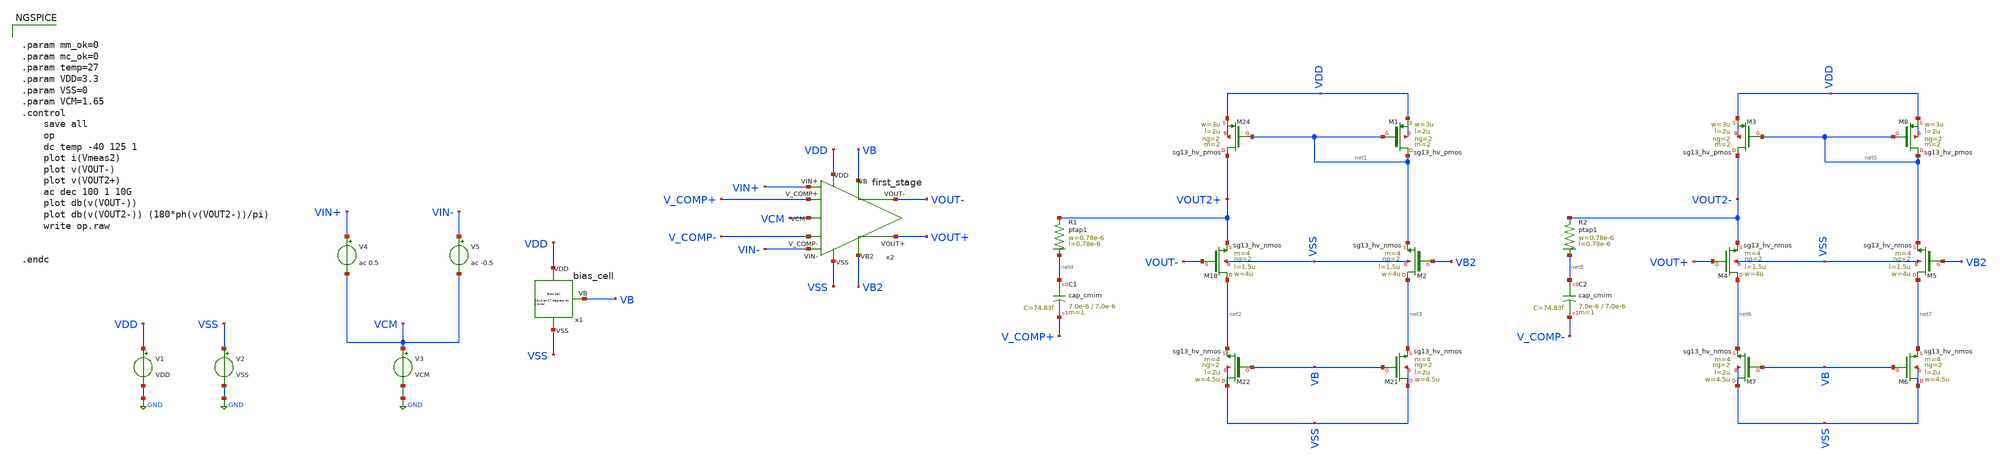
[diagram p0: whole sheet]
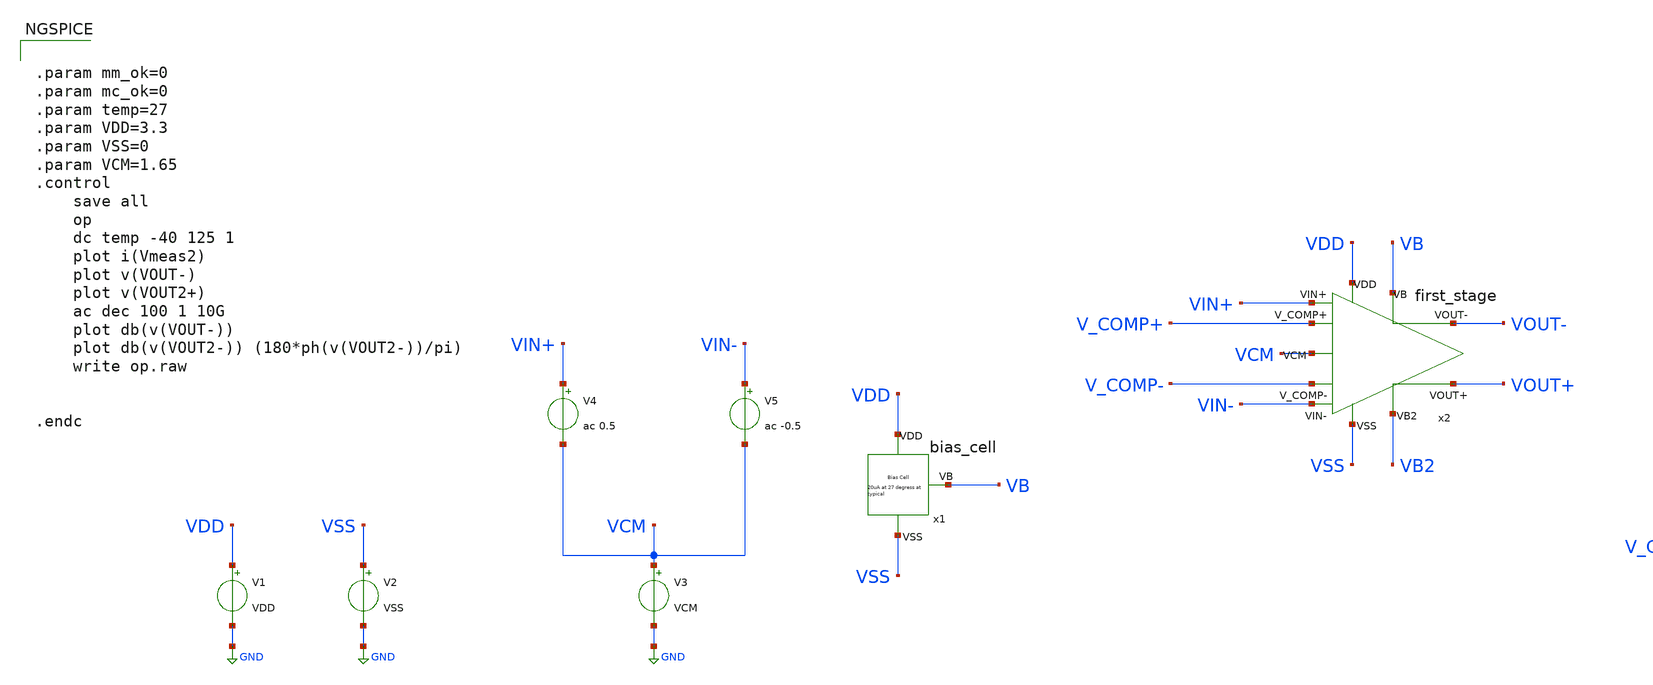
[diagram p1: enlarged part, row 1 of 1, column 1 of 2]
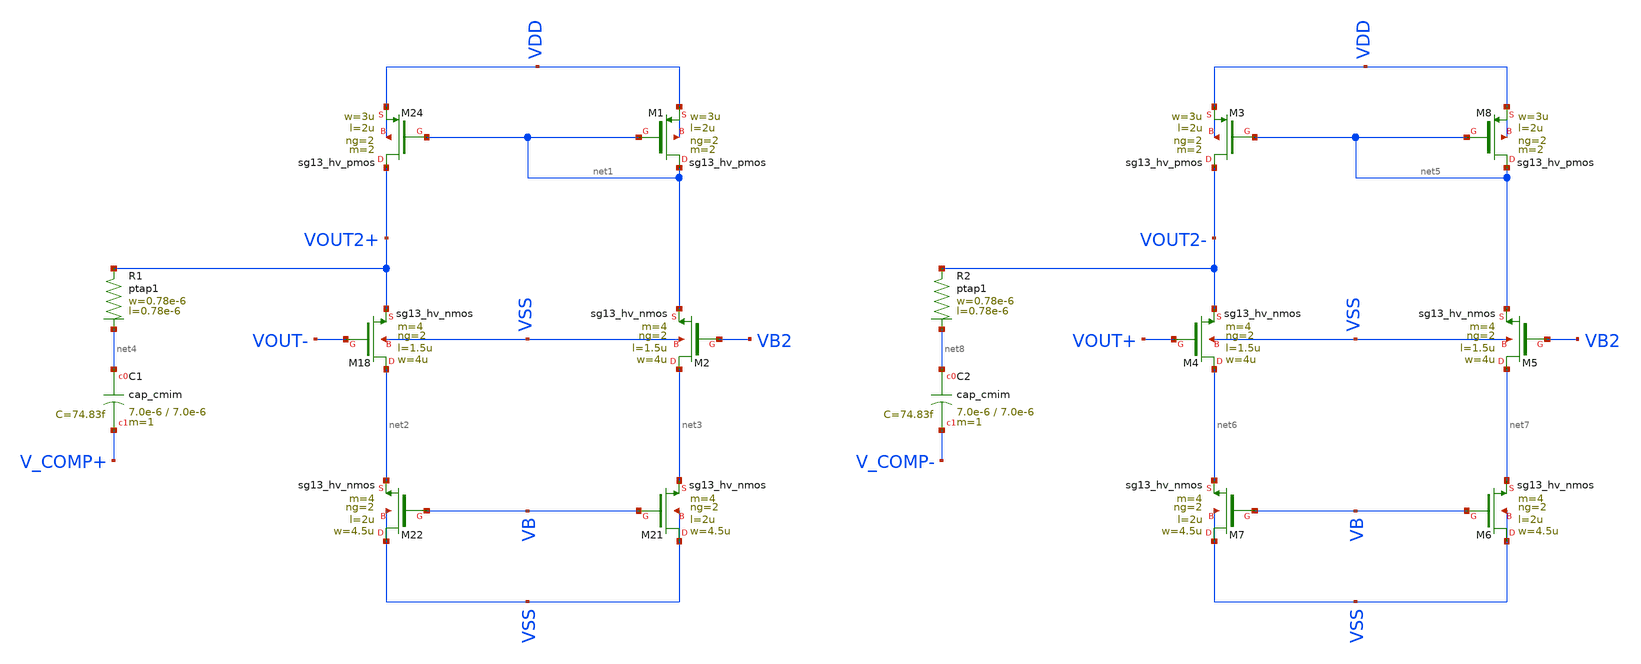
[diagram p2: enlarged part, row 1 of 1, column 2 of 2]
** sch_path: Learning/fully_differencial/Indirect_Compensation_Techniques_for_Three_Stage_Fully_Differential_Op_amps_IHP130/testbenches/first_stage_sim.sch
**.subckt first_stage_sim
x1 VDD VSS VB bias_cell
V1 VDD GND VDD
V2 VSS GND VSS
V3 VCM GND VCM
V4 VIN+ VCM ac 0.5
V5 VIN- VCM ac -0.5
x2 VDD VSS VB VIN+ VIN- VOUT- VOUT+ VB2 VCM V_COMP+ V_COMP- first_stage
XM24 VOUT2+ net1 VDD VDD sg13_hv_pmos w=3u l=2u ng=2 m=2 mm_ok=1
XM18 net2 VOUT- VOUT2+ VSS sg13_hv_nmos w=4u l=1.5u ng=2 m=4 mm_ok=1
XM2 net3 VB2 net1 VSS sg13_hv_nmos w=4u l=1.5u ng=2 m=4 mm_ok=1
XM21 VSS VB net3 VSS sg13_hv_nmos w=4.5u l=2u ng=2 m=4 mm_ok=1
XM22 VSS VB net2 VSS sg13_hv_nmos w=4.5u l=2u ng=2 m=4 mm_ok=1
XM1 net1 net1 VDD VDD sg13_hv_pmos w=3u l=2u ng=2 m=2 mm_ok=1
XC1 net4 V_COMP+ cap_cmim w=7.0e-6 l=7.0e-6 m=1 mm_ok=1
XR1 VOUT2+ net4 ptap1 R=262.8 w=0.78e-6 l=0.78e-6
XM3 VOUT2- net5 VDD VDD sg13_hv_pmos w=3u l=2u ng=2 m=2 mm_ok=1
XM4 net6 VOUT+ VOUT2- VSS sg13_hv_nmos w=4u l=1.5u ng=2 m=4 mm_ok=1
XM5 net7 VB2 net5 VSS sg13_hv_nmos w=4u l=1.5u ng=2 m=4 mm_ok=1
XM6 VSS VB net7 VSS sg13_hv_nmos w=4.5u l=2u ng=2 m=4 mm_ok=1
XM7 VSS VB net6 VSS sg13_hv_nmos w=4.5u l=2u ng=2 m=4 mm_ok=1
XM8 net5 net5 VDD VDD sg13_hv_pmos w=3u l=2u ng=2 m=2 mm_ok=1
XC2 net8 V_COMP- cap_cmim w=7.0e-6 l=7.0e-6 m=1 mm_ok=1
XR2 VOUT2- net8 ptap1 R=262.8 w=0.78e-6 l=0.78e-6
**** begin user architecture code


.param mm_ok=0
.param mc_ok=0
.param temp=27
.param VDD=3.3
.param VSS=0
.param VCM=1.65
.control
	save all
	op
	dc temp -40 125 1
	plot i(Vmeas2)
	plot v(VOUT-)
	plot v(VOUT2+)
	ac dec 100 1 10G
	plot db(v(VOUT-))
	plot db(v(VOUT2-)) (180*ph(v(VOUT2-))/pi)
	write op.raw


.endc



.lib cornerMOShv.lib mos_tt


.lib $::SG13G2_MODELS/cornerRES.lib res_typ


.lib $::SG13G2_MODELS/cornerCAP.lib cap_typ

**** end user architecture code
**.ends
.GLOBAL GND
.end
